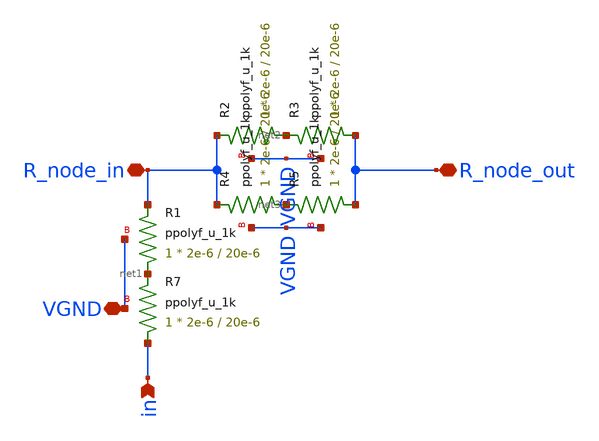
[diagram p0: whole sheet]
** sch_path: xschem/dac_sub_r2r.sch
**.subckt dac_sub_r2r in R_node_out R_node_in VGND
*.ipin in
*.iopin R_node_out
*.iopin R_node_in
*.iopin VGND
XR7 in net1 VGND ppolyf_u_1k r_width=2e-6 r_length=20e-6 m=1
XR1 net1 R_node_in VGND ppolyf_u_1k r_width=2e-6 r_length=20e-6 m=1
XR2 net2 R_node_in VGND ppolyf_u_1k r_width=2e-6 r_length=20e-6 m=1
XR3 R_node_out net2 VGND ppolyf_u_1k r_width=2e-6 r_length=20e-6 m=1
XR4 net3 R_node_in VGND ppolyf_u_1k r_width=2e-6 r_length=20e-6 m=1
XR5 R_node_out net3 VGND ppolyf_u_1k r_width=2e-6 r_length=20e-6 m=1
**.ends
.end
